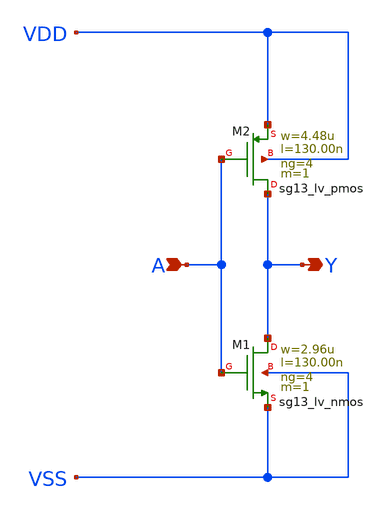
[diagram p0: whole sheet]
** sch_path: ihp-sg13g2/libs.ref/sg13g2_stdcell/sch/xschem/sg13g2_inv_4.sch
* Copyright 2023 IHP PDK Authors
* Licensed under the Apache License, Version 2.0 (the "License");
* you may not use this file except in compliance with the License.
* You may obtain a copy of the License at
* https://www.apache.org/licenses/LICENSE-2.0
* Unless required by applicable law or agreed to in writing, software
* distributed under the License is distributed on an "AS IS" BASIS,
* WITHOUT WARRANTIES OR CONDITIONS OF ANY KIND, either express or implied.
* See the License for the specific language governing permissions and
* limitations under the License.
**.subckt sg13g2_inv_4 A Y
*.ipin A
*.opin Y
XM1 Y A VSS VSS sg13_lv_nmos w=2.96u l=130.00n ng=4 m=1 mm_ok=1
XM2 Y A VDD VDD sg13_lv_pmos w=4.48u l=130.00n ng=4 m=1 mm_ok=1
**.ends
.end
